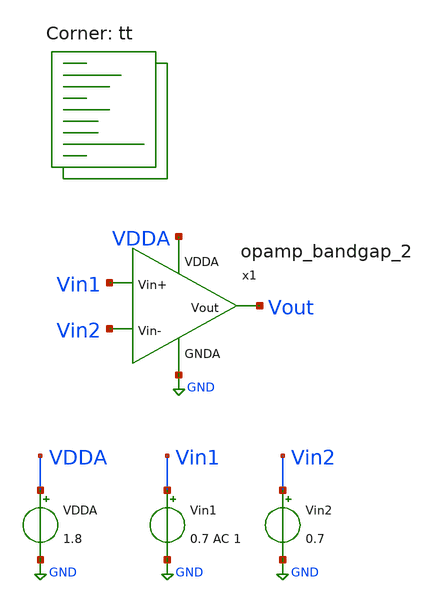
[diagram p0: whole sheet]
** sch_path: projects/bandgapref/xschem_ngspice/new_files/tb_opamp_bandgap.sch
**.subckt tb_opamp_bandgap
VDDA VDDA GND 1.8
Vin1 Vin1 GND 0.7 AC 1
Vin2 Vin2 GND 0.7
x1 VDDA Vout Vin2 Vin1 GND opamp_bandgap_2
**** begin user architecture code



.option wnflag=1
.option savecurrents

* .param VDDGAUSS = agauss(1.8, 0.05, 1)
* .param VDD = VDDGAUSS
* .param VDD = 1.8

* .param TEMPGAUSS = agauss(40, 30, 1)
* .param temp = TEMPGAUSS
.option temp = 26

.save @m.x1.xm1.msky130_fd_pr__nfet_01v8[gm] @m.x1.xm2.msky130_fd_pr__nfet_01v8[gm] @m.x1.xm3.msky130_fd_pr__nfet_01v8[gm] @m.x1.xm4.msky130_fd_pr__pfet_01v8[gm] @m.x1.xm5.msky130_fd_pr__pfet_01v8[gm] @m.x1.xm6.msky130_fd_pr__nfet_01v8[gm] @m.x1.xm7.msky130_fd_pr__pfet_01v8[gm]

.control

  save all
   *tran 1u 20m
   ac dec 20 1 1T

  write tb_opamp_bandgap.raw
  set appendwrite

.endc



.lib $::SKYWATER_MODELS/sky130.lib.spice tt
**** end user architecture code
**.ends

* expanding   symbol:  opamp_bandgap_2.sym # of pins=5
** sym_path: projects/bandgapref/xschem_ngspice/new_files/opamp_bandgap_2.sym
** sch_path: projects/bandgapref/xschem_ngspice/new_files/opamp_bandgap_2.sch
.subckt opamp_bandgap_2 VDDA Vout Vin- Vin+ GNDA
*.ipin Vin+
*.opin Vout
*.ipin Vin-
*.ipin GNDA
*.ipin VDDA
XM1 V_p VDDA GNDA GNDA sky130_fd_pr__nfet_01v8 L=10 W=5 nf=1 ad='int((nf+1)/2) * W/nf * 0.29' as='int((nf+2)/2) * W/nf * 0.29'
+ pd='2*int((nf+1)/2) * (W/nf + 0.29)' ps='2*int((nf+2)/2) * (W/nf + 0.29)' nrd='0.29 / W' nrs='0.29 / W'
+ sa=0 sb=0 sd=0 mult=1 m=1
XM2 V_mirror Vin- V_p GNDA sky130_fd_pr__nfet_01v8 L=0.2 W=5 nf=1 ad='int((nf+1)/2) * W/nf * 0.29' as='int((nf+2)/2) * W/nf * 0.29'
+ pd='2*int((nf+1)/2) * (W/nf + 0.29)' ps='2*int((nf+2)/2) * (W/nf + 0.29)' nrd='0.29 / W' nrs='0.29 / W'
+ sa=0 sb=0 sd=0 mult=1 m=1
XM3 1st_Vout Vin+ V_p GNDA sky130_fd_pr__nfet_01v8 L=0.2 W=5 nf=1 ad='int((nf+1)/2) * W/nf * 0.29' as='int((nf+2)/2) * W/nf * 0.29'
+ pd='2*int((nf+1)/2) * (W/nf + 0.29)' ps='2*int((nf+2)/2) * (W/nf + 0.29)' nrd='0.29 / W' nrs='0.29 / W'
+ sa=0 sb=0 sd=0 mult=1 m=1
XM5 V_mirror V_mirror VDDA VDDA sky130_fd_pr__pfet_01v8 L=0.2 W=10 nf=2 ad='int((nf+1)/2) * W/nf * 0.29'
+ as='int((nf+2)/2) * W/nf * 0.29' pd='2*int((nf+1)/2) * (W/nf + 0.29)' ps='2*int((nf+2)/2) * (W/nf + 0.29)'
+ nrd='0.29 / W' nrs='0.29 / W' sa=0 sb=0 sd=0 mult=1 m=1
XM6 1st_Vout V_mirror VDDA VDDA sky130_fd_pr__pfet_01v8 L=0.2 W=10 nf=2 ad='int((nf+1)/2) * W/nf * 0.29'
+ as='int((nf+2)/2) * W/nf * 0.29' pd='2*int((nf+1)/2) * (W/nf + 0.29)' ps='2*int((nf+2)/2) * (W/nf + 0.29)'
+ nrd='0.29 / W' nrs='0.29 / W' sa=0 sb=0 sd=0 mult=1 m=1
XM4 Vout VDDA GNDA GNDA sky130_fd_pr__nfet_01v8 L=10 W=5 nf=1 ad='int((nf+1)/2) * W/nf * 0.29' as='int((nf+2)/2) * W/nf * 0.29'
+ pd='2*int((nf+1)/2) * (W/nf + 0.29)' ps='2*int((nf+2)/2) * (W/nf + 0.29)' nrd='0.29 / W' nrs='0.29 / W'
+ sa=0 sb=0 sd=0 mult=1 m=1
XM7 Vout 1st_Vout VDDA VDDA sky130_fd_pr__pfet_01v8 L=0.2 W=10 nf=2 ad='int((nf+1)/2) * W/nf * 0.29'
+ as='int((nf+2)/2) * W/nf * 0.29' pd='2*int((nf+1)/2) * (W/nf + 0.29)' ps='2*int((nf+2)/2) * (W/nf + 0.29)'
+ nrd='0.29 / W' nrs='0.29 / W' sa=0 sb=0 sd=0 mult=1 m=1
.ends

.GLOBAL GND
.end
